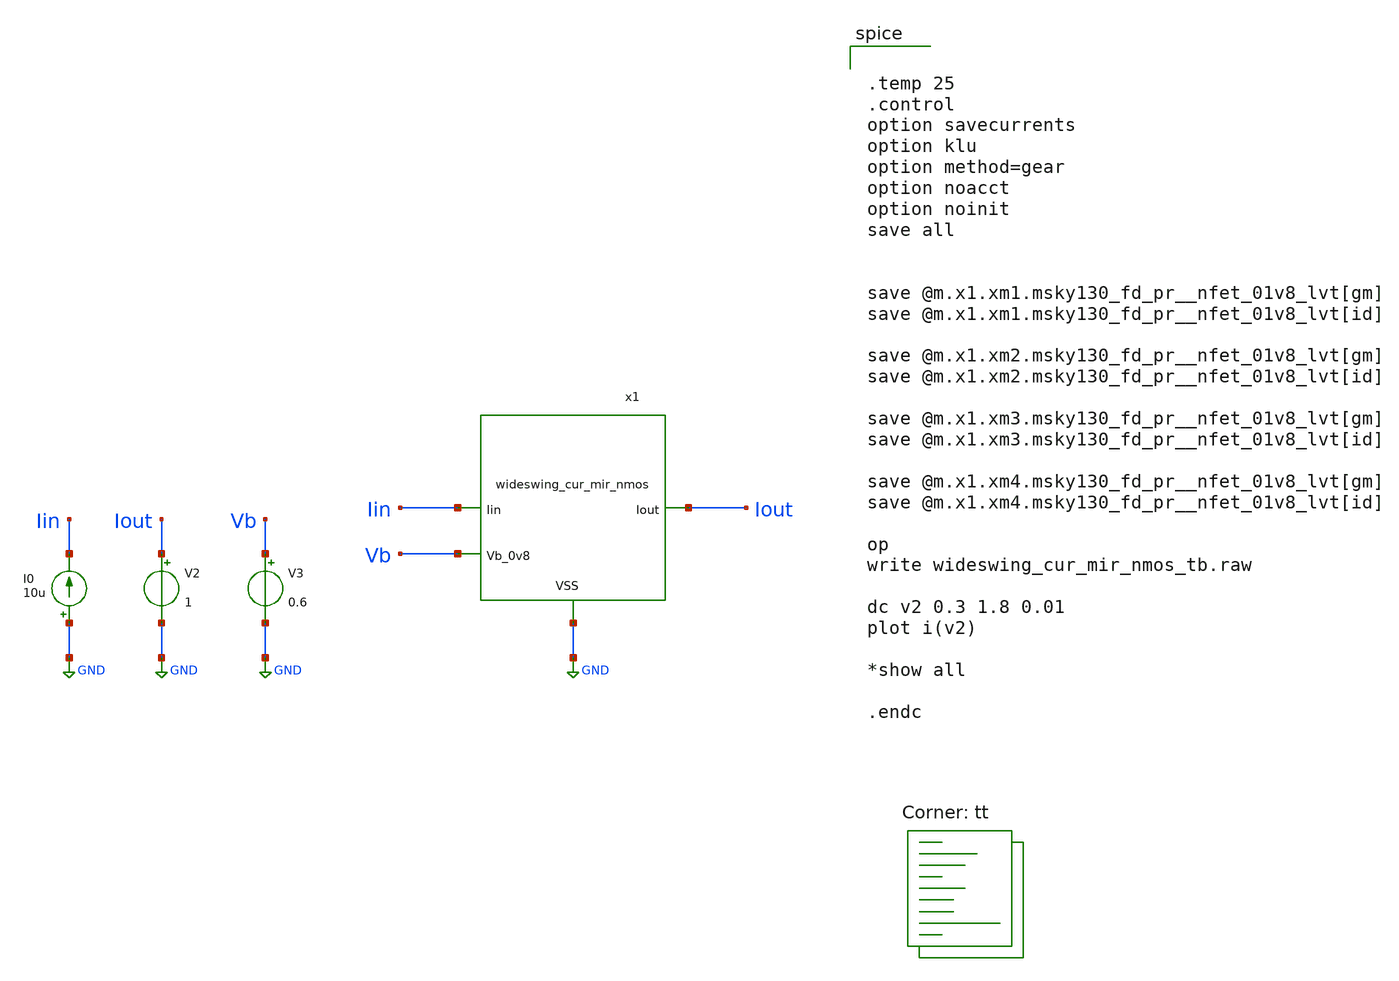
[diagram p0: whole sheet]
** sch_path: xschem/wideswing_cur_mir_nmos_tb.sch
**.subckt wideswing_cur_mir_nmos_tb
I0 GND Iin 10u
V2 Iout GND 1
.save i(v2)
V3 Vb GND 0.6
.save i(v3)
x1 GND Vb Iin Iout wideswing_cur_mir_nmos
**** begin user architecture code


.temp 25
.control
option savecurrents
option klu
option method=gear
option noacct
option noinit
save all


save @m.x1.xm1.msky130_fd_pr__nfet_01v8_lvt[gm]
save @m.x1.xm1.msky130_fd_pr__nfet_01v8_lvt[id]

save @m.x1.xm2.msky130_fd_pr__nfet_01v8_lvt[gm]
save @m.x1.xm2.msky130_fd_pr__nfet_01v8_lvt[id]

save @m.x1.xm3.msky130_fd_pr__nfet_01v8_lvt[gm]
save @m.x1.xm3.msky130_fd_pr__nfet_01v8_lvt[id]

save @m.x1.xm4.msky130_fd_pr__nfet_01v8_lvt[gm]
save @m.x1.xm4.msky130_fd_pr__nfet_01v8_lvt[id]

op
write wideswing_cur_mir_nmos_tb.raw

dc v2 0.3 1.8 0.01
plot i(v2)

*show all

.endc

.lib $::SKYWATER_MODELS/sky130.lib.spice tt
**** end user architecture code
**.ends

* expanding   symbol:  wideswing_cur_mir_nmos.sym # of pins=4
** sym_path: xschem/wideswing_cur_mir_nmos.sym
** sch_path: xschem/wideswing_cur_mir_nmos.sch
.subckt wideswing_cur_mir_nmos VSS Vb_0v8 Iin Iout
*.ipin Iin
*.opin Iout
*.ipin Vb_0v8
*.iopin VSS
XM1 net1 Iin VSS VSS sky130_fd_pr__nfet_01v8_lvt L=8 W=100 nf=1 ad='int((1 + 1)/2) * 100 / 1 * 0.29'
+ as='int((1 + 2)/2) * 100 / 1 * 0.29' pd='2*int((1 + 1)/2) * (100 / 1 + 0.29)' ps='2*int((1 + 2)/2) * (100 / 1 + 0.29)'
+ nrd='0.29 / 100 ' nrs='0.29 / 100 ' sa=0 sb=0 sd=0 mult=1 m=1
XM2 net2 Iin VSS VSS sky130_fd_pr__nfet_01v8_lvt L=8 W=100 nf=1 ad='int((1 + 1)/2) * 100 / 1 * 0.29'
+ as='int((1 + 2)/2) * 100 / 1 * 0.29' pd='2*int((1 + 1)/2) * (100 / 1 + 0.29)' ps='2*int((1 + 2)/2) * (100 / 1 + 0.29)'
+ nrd='0.29 / 100 ' nrs='0.29 / 100 ' sa=0 sb=0 sd=0 mult=1 m=1
XM3 Iin Vb_0v8 net1 VSS sky130_fd_pr__nfet_01v8_lvt L=8 W=100 nf=1 ad='int((1 + 1)/2) * 100 / 1 * 0.29'
+ as='int((1 + 2)/2) * 100 / 1 * 0.29' pd='2*int((1 + 1)/2) * (100 / 1 + 0.29)' ps='2*int((1 + 2)/2) * (100 / 1 + 0.29)'
+ nrd='0.29 / 100 ' nrs='0.29 / 100 ' sa=0 sb=0 sd=0 mult=1 m=1
XM4 Iout Vb_0v8 net2 VSS sky130_fd_pr__nfet_01v8_lvt L=8 W=100 nf=1 ad='int((1 + 1)/2) * 100 / 1 * 0.29'
+ as='int((1 + 2)/2) * 100 / 1 * 0.29' pd='2*int((1 + 1)/2) * (100 / 1 + 0.29)' ps='2*int((1 + 2)/2) * (100 / 1 + 0.29)'
+ nrd='0.29 / 100 ' nrs='0.29 / 100 ' sa=0 sb=0 sd=0 mult=1 m=1
.ends

.GLOBAL GND
.end
